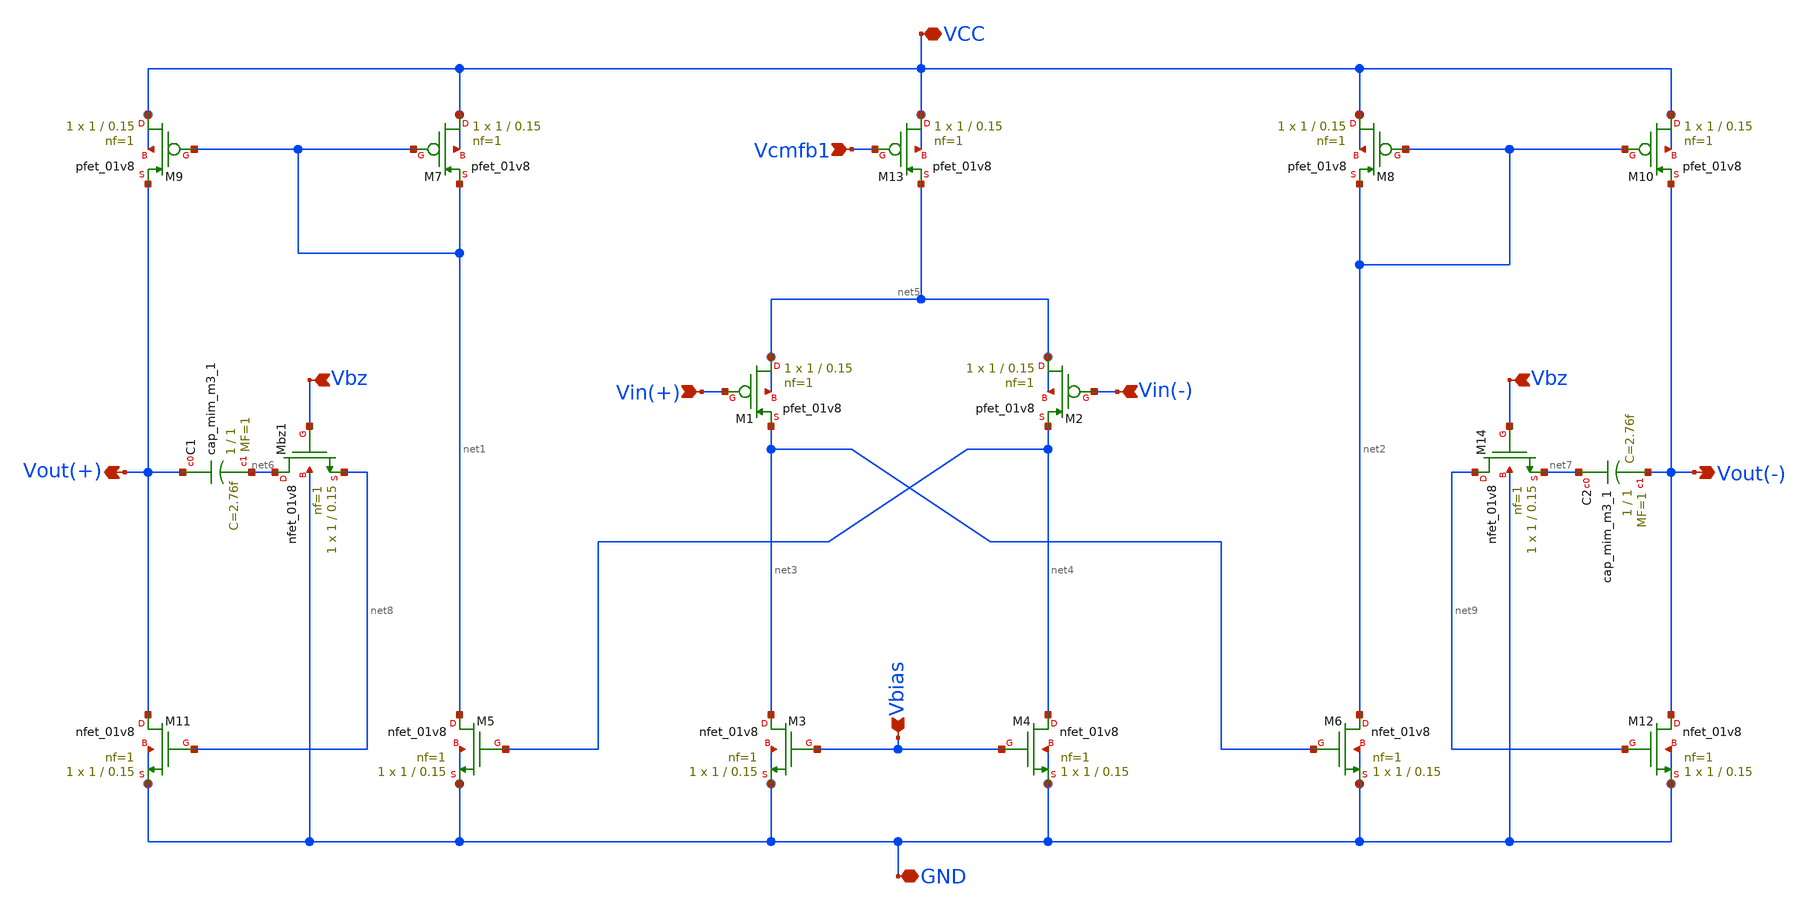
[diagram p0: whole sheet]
** sch_path: blocks/01_OTA/xschem/OTA.sch
**.subckt OTA Vin(+) Vin(-) Vbias Vbz Vbz Vcmfb1 Vout(+) Vout(-) VCC GND
*.ipin Vin(+)
*.ipin Vin(-)
*.ipin Vbias
*.ipin Vbz
*.ipin Vbz
*.ipin Vcmfb1
*.opin Vout(+)
*.opin Vout(-)
*.iopin VCC
*.iopin GND
XM1 net5 Vin(+) net3 net5 sky130_fd_pr__pfet_01v8 L=0.15 W=1 nf=1 ad='int((1 + 1)/2) * 1 / 1 * 0.29'
+ as='int((1 + 2)/2) * 1 / 1 * 0.29' pd='2*int((1 + 1)/2) * (1 / 1 + 0.29)' ps='2*int((1 + 2)/2) * (1 / 1 + 0.29)'
+ nrd='0.29 / 1 ' nrs='0.29 / 1 ' sa=0 sb=0 sd=0 mult=1 m=1
XM2 net5 Vin(-) net4 net5 sky130_fd_pr__pfet_01v8 L=0.15 W=1 nf=1 ad='int((1 + 1)/2) * 1 / 1 * 0.29'
+ as='int((1 + 2)/2) * 1 / 1 * 0.29' pd='2*int((1 + 1)/2) * (1 / 1 + 0.29)' ps='2*int((1 + 2)/2) * (1 / 1 + 0.29)'
+ nrd='0.29 / 1 ' nrs='0.29 / 1 ' sa=0 sb=0 sd=0 mult=1 m=1
XM3 net3 Vbias GND GND sky130_fd_pr__nfet_01v8 L=0.15 W=1 nf=1 ad='int((1 + 1)/2) * 1 / 1 * 0.29' as='int((1 + 2)/2) * 1 / 1 * 0.29'
+ pd='2*int((1 + 1)/2) * (1 / 1 + 0.29)' ps='2*int((1 + 2)/2) * (1 / 1 + 0.29)' nrd='0.29 / 1 ' nrs='0.29 / 1 '
+ sa=0 sb=0 sd=0 mult=1 m=1
XM4 net4 Vbias GND GND sky130_fd_pr__nfet_01v8 L=0.15 W=1 nf=1 ad='int((1 + 1)/2) * 1 / 1 * 0.29' as='int((1 + 2)/2) * 1 / 1 * 0.29'
+ pd='2*int((1 + 1)/2) * (1 / 1 + 0.29)' ps='2*int((1 + 2)/2) * (1 / 1 + 0.29)' nrd='0.29 / 1 ' nrs='0.29 / 1 '
+ sa=0 sb=0 sd=0 mult=1 m=1
XM5 net1 net4 GND GND sky130_fd_pr__nfet_01v8 L=0.15 W=1 nf=1 ad='int((1 + 1)/2) * 1 / 1 * 0.29' as='int((1 + 2)/2) * 1 / 1 * 0.29'
+ pd='2*int((1 + 1)/2) * (1 / 1 + 0.29)' ps='2*int((1 + 2)/2) * (1 / 1 + 0.29)' nrd='0.29 / 1 ' nrs='0.29 / 1 '
+ sa=0 sb=0 sd=0 mult=1 m=1
XM6 net2 net3 GND GND sky130_fd_pr__nfet_01v8 L=0.15 W=1 nf=1 ad='int((1 + 1)/2) * 1 / 1 * 0.29' as='int((1 + 2)/2) * 1 / 1 * 0.29'
+ pd='2*int((1 + 1)/2) * (1 / 1 + 0.29)' ps='2*int((1 + 2)/2) * (1 / 1 + 0.29)' nrd='0.29 / 1 ' nrs='0.29 / 1 '
+ sa=0 sb=0 sd=0 mult=1 m=1
XM7 VCC net1 net1 VCC sky130_fd_pr__pfet_01v8 L=0.15 W=1 nf=1 ad='int((1 + 1)/2) * 1 / 1 * 0.29' as='int((1 + 2)/2) * 1 / 1 * 0.29'
+ pd='2*int((1 + 1)/2) * (1 / 1 + 0.29)' ps='2*int((1 + 2)/2) * (1 / 1 + 0.29)' nrd='0.29 / 1 ' nrs='0.29 / 1 '
+ sa=0 sb=0 sd=0 mult=1 m=1
XM8 VCC net2 net2 VCC sky130_fd_pr__pfet_01v8 L=0.15 W=1 nf=1 ad='int((1 + 1)/2) * 1 / 1 * 0.29' as='int((1 + 2)/2) * 1 / 1 * 0.29'
+ pd='2*int((1 + 1)/2) * (1 / 1 + 0.29)' ps='2*int((1 + 2)/2) * (1 / 1 + 0.29)' nrd='0.29 / 1 ' nrs='0.29 / 1 '
+ sa=0 sb=0 sd=0 mult=1 m=1
XM9 VCC net1 Vout(+) VCC sky130_fd_pr__pfet_01v8 L=0.15 W=1 nf=1 ad='int((1 + 1)/2) * 1 / 1 * 0.29' as='int((1 + 2)/2) * 1 / 1 * 0.29'
+ pd='2*int((1 + 1)/2) * (1 / 1 + 0.29)' ps='2*int((1 + 2)/2) * (1 / 1 + 0.29)' nrd='0.29 / 1 ' nrs='0.29 / 1 '
+ sa=0 sb=0 sd=0 mult=1 m=1
XM10 VCC net2 Vout(-) VCC sky130_fd_pr__pfet_01v8 L=0.15 W=1 nf=1 ad='int((1 + 1)/2) * 1 / 1 * 0.29'
+ as='int((1 + 2)/2) * 1 / 1 * 0.29' pd='2*int((1 + 1)/2) * (1 / 1 + 0.29)' ps='2*int((1 + 2)/2) * (1 / 1 + 0.29)'
+ nrd='0.29 / 1 ' nrs='0.29 / 1 ' sa=0 sb=0 sd=0 mult=1 m=1
XM11 Vout(+) net8 GND GND sky130_fd_pr__nfet_01v8 L=0.15 W=1 nf=1 ad='int((1 + 1)/2) * 1 / 1 * 0.29'
+ as='int((1 + 2)/2) * 1 / 1 * 0.29' pd='2*int((1 + 1)/2) * (1 / 1 + 0.29)' ps='2*int((1 + 2)/2) * (1 / 1 + 0.29)'
+ nrd='0.29 / 1 ' nrs='0.29 / 1 ' sa=0 sb=0 sd=0 mult=1 m=1
XM12 Vout(-) net9 GND GND sky130_fd_pr__nfet_01v8 L=0.15 W=1 nf=1 ad='int((1 + 1)/2) * 1 / 1 * 0.29'
+ as='int((1 + 2)/2) * 1 / 1 * 0.29' pd='2*int((1 + 1)/2) * (1 / 1 + 0.29)' ps='2*int((1 + 2)/2) * (1 / 1 + 0.29)'
+ nrd='0.29 / 1 ' nrs='0.29 / 1 ' sa=0 sb=0 sd=0 mult=1 m=1
XM13 VCC Vcmfb1 net5 VCC sky130_fd_pr__pfet_01v8 L=0.15 W=1 nf=1 ad='int((1 + 1)/2) * 1 / 1 * 0.29' as='int((1 + 2)/2) * 1 / 1 * 0.29'
+ pd='2*int((1 + 1)/2) * (1 / 1 + 0.29)' ps='2*int((1 + 2)/2) * (1 / 1 + 0.29)' nrd='0.29 / 1 ' nrs='0.29 / 1 '
+ sa=0 sb=0 sd=0 mult=1 m=1
XC1 Vout(+) net6 sky130_fd_pr__cap_mim_m3_1 W=1 L=1 MF=1 m=1
XMbz1 net6 Vbz net8 GND sky130_fd_pr__nfet_01v8 L=0.15 W=1 nf=1 ad='int((1 + 1)/2) * 1 / 1 * 0.29' as='int((1 + 2)/2) * 1 / 1 * 0.29'
+ pd='2*int((1 + 1)/2) * (1 / 1 + 0.29)' ps='2*int((1 + 2)/2) * (1 / 1 + 0.29)' nrd='0.29 / 1 ' nrs='0.29 / 1 '
+ sa=0 sb=0 sd=0 mult=1 m=1
XC2 net7 Vout(-) sky130_fd_pr__cap_mim_m3_1 W=1 L=1 MF=1 m=1
XM14 net9 Vbz net7 GND sky130_fd_pr__nfet_01v8 L=0.15 W=1 nf=1 ad='int((1 + 1)/2) * 1 / 1 * 0.29' as='int((1 + 2)/2) * 1 / 1 * 0.29'
+ pd='2*int((1 + 1)/2) * (1 / 1 + 0.29)' ps='2*int((1 + 2)/2) * (1 / 1 + 0.29)' nrd='0.29 / 1 ' nrs='0.29 / 1 '
+ sa=0 sb=0 sd=0 mult=1 m=1
**.ends
.end
